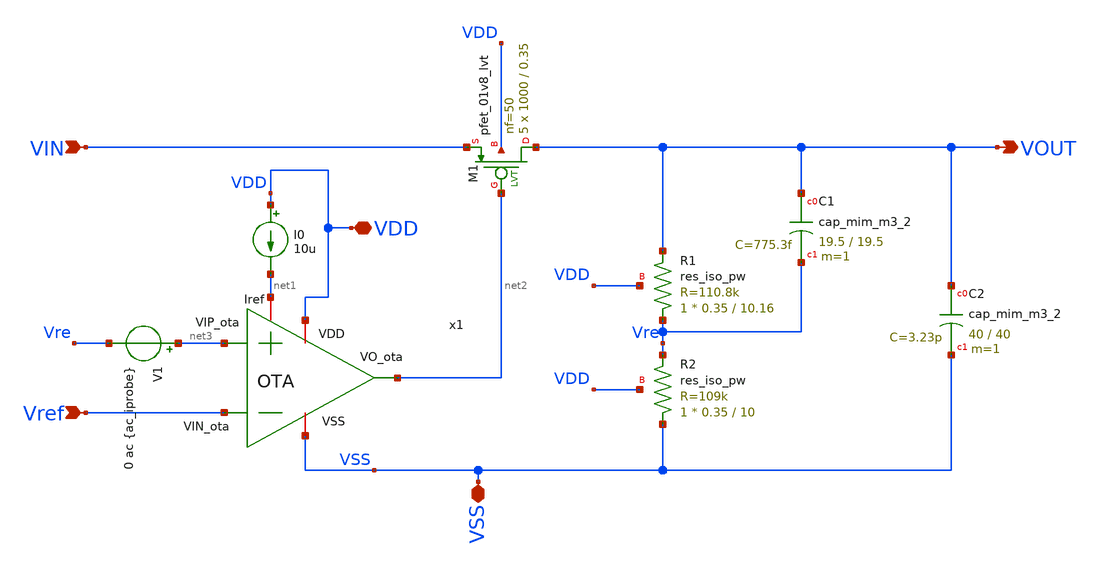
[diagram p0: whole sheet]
** sch_path: xschem/LDO.sch
**.subckt LDO VIN VDD VOUT Vref VSS
*.ipin VIN
*.iopin VDD
*.opin VOUT
*.ipin Vref
*.iopin VSS
x1 VDD net2 Vref net3 net1 VSS OTA
I0 VDD net1 10u
XM1 VOUT net2 VIN VDD sky130_fd_pr__pfet_01v8_lvt L=0.35 W=1000 nf=50 ad='int((50 + 1)/2) * 1000 / 50 * 0.29'
+ as='int((50 + 2)/2) * 1000 / 50 * 0.29' pd='2*int((50 + 1)/2) * (1000 / 50 + 0.29)' ps='2*int((50 + 2)/2) * (1000 / 50 + 0.29)'
+ nrd='0.29 / 1000 ' nrs='0.29 / 1000 ' sa=0 sb=0 sd=0 mult=5 m=5
XR1 Vre VOUT VDD sky130_fd_pr__res_iso_pw W=0.35 L=10.16 m=1
XR2 VSS Vre VDD sky130_fd_pr__res_iso_pw W=0.35 L=10 m=1
V1 net3 Vre 0 ac {ac_iprobe}
XC1 VOUT Vre sky130_fd_pr__cap_mim_m3_2 W=19.5 L=19.5 MF=1 m=1
XC2 VOUT VSS sky130_fd_pr__cap_mim_m3_2 W=40 L=40 MF=1 m=1
**.ends

* expanding   symbol:  /foss/designs/LDO-sky130/xschem/OTA.sym # of pins=6
** sym_path: xschem/OTA.sym
** sch_path: xschem/OTA.sch
.subckt OTA VDD VO_ota VIN_ota VIP_ota Iref VSS
*.ipin VIN_ota
*.opin VO_ota
*.iopin Iref
*.iopin VSS
*.iopin VDD
*.ipin VIP_ota
XR1 VO_ota1 net1 VDD sky130_fd_pr__res_high_po W=0.35 L=360 mult=1 m=1
XC1 VO_ota net1 sky130_fd_pr__cap_mim_m3_2 W=50 L=50 MF=1 m=1
XMpr VO_ota1 net2 VSS VSS sky130_fd_pr__nfet_01v8 L=0.5 W=3 nf=1 ad='int((1 + 1)/2) * 3 / 1 * 0.29' as='int((1 + 2)/2) * 3 / 1 * 0.29'
+ pd='2*int((1 + 1)/2) * (3 / 1 + 0.29)' ps='2*int((1 + 2)/2) * (3 / 1 + 0.29)' nrd='0.29 / 3 ' nrs='0.29 / 3 '
+ sa=0 sb=0 sd=0 mult=1 m=1
XMnr net2 net2 VSS VSS sky130_fd_pr__nfet_01v8 L=0.5 W=3 nf=1 ad='int((1 + 1)/2) * 3 / 1 * 0.29' as='int((1 + 2)/2) * 3 / 1 * 0.29'
+ pd='2*int((1 + 1)/2) * (3 / 1 + 0.29)' ps='2*int((1 + 2)/2) * (3 / 1 + 0.29)' nrd='0.29 / 3 ' nrs='0.29 / 3 '
+ sa=0 sb=0 sd=0 mult=1 m=1
XMn net2 VIN_ota Vtail VDD sky130_fd_pr__pfet_01v8 L=0.5 W=28 nf=1 ad='int((1 + 1)/2) * 28 / 1 * 0.29'
+ as='int((1 + 2)/2) * 28 / 1 * 0.29' pd='2*int((1 + 1)/2) * (28 / 1 + 0.29)' ps='2*int((1 + 2)/2) * (28 / 1 + 0.29)'
+ nrd='0.29 / 28 ' nrs='0.29 / 28 ' sa=0 sb=0 sd=0 mult=1 m=1
XMp VO_ota1 VIP_ota Vtail VDD sky130_fd_pr__pfet_01v8 L=0.5 W=28 nf=1 ad='int((1 + 1)/2) * 28 / 1 * 0.29'
+ as='int((1 + 2)/2) * 28 / 1 * 0.29' pd='2*int((1 + 1)/2) * (28 / 1 + 0.29)' ps='2*int((1 + 2)/2) * (28 / 1 + 0.29)'
+ nrd='0.29 / 28 ' nrs='0.29 / 28 ' sa=0 sb=0 sd=0 mult=1 m=1
XMo VO_ota VO_ota1 VSS VSS sky130_fd_pr__nfet_01v8 L=0.5 W=3 nf=1 ad='int((1 + 1)/2) * 3 / 1 * 0.29'
+ as='int((1 + 2)/2) * 3 / 1 * 0.29' pd='2*int((1 + 1)/2) * (3 / 1 + 0.29)' ps='2*int((1 + 2)/2) * (3 / 1 + 0.29)'
+ nrd='0.29 / 3 ' nrs='0.29 / 3 ' sa=0 sb=0 sd=0 mult=1 m=1
XMc3 VGP Iref VSS VSS sky130_fd_pr__nfet_01v8 L=0.5 W=1 nf=1 ad='int((1 + 1)/2) * 1 / 1 * 0.29' as='int((1 + 2)/2) * 1 / 1 * 0.29'
+ pd='2*int((1 + 1)/2) * (1 / 1 + 0.29)' ps='2*int((1 + 2)/2) * (1 / 1 + 0.29)' nrd='0.29 / 1 ' nrs='0.29 / 1 '
+ sa=0 sb=0 sd=0 mult=1 m=1
XMp2 Iref Iref VSS VSS sky130_fd_pr__nfet_01v8 L=0.5 W=1 nf=1 ad='int((1 + 1)/2) * 1 / 1 * 0.29' as='int((1 + 2)/2) * 1 / 1 * 0.29'
+ pd='2*int((1 + 1)/2) * (1 / 1 + 0.29)' ps='2*int((1 + 2)/2) * (1 / 1 + 0.29)' nrd='0.29 / 1 ' nrs='0.29 / 1 '
+ sa=0 sb=0 sd=0 mult=1 m=1
XMr VGP VGP VDD VDD sky130_fd_pr__pfet_01v8_lvt L=0.5 W=2.4 nf=1 ad='int((1 + 1)/2) * 2.4 / 1 * 0.29'
+ as='int((1 + 2)/2) * 2.4 / 1 * 0.29' pd='2*int((1 + 1)/2) * (2.4 / 1 + 0.29)' ps='2*int((1 + 2)/2) * (2.4 / 1 + 0.29)'
+ nrd='0.29 / 2.4 ' nrs='0.29 / 2.4 ' sa=0 sb=0 sd=0 mult=1 m=1
XMrc1 Vtail VGP VDD VDD sky130_fd_pr__pfet_01v8_lvt L=0.5 W=19.4 nf=1 ad='int((1 + 1)/2) * 19.4 / 1 * 0.29'
+ as='int((1 + 2)/2) * 19.4 / 1 * 0.29' pd='2*int((1 + 1)/2) * (19.4 / 1 + 0.29)' ps='2*int((1 + 2)/2) * (19.4 / 1 + 0.29)'
+ nrd='0.29 / 19.4 ' nrs='0.29 / 19.4 ' sa=0 sb=0 sd=0 mult=1 m=1
XMrc2 VO_ota VGP VDD VDD sky130_fd_pr__pfet_01v8_lvt L=0.5 W=8 nf=1 ad='int((1 + 1)/2) * 8 / 1 * 0.29'
+ as='int((1 + 2)/2) * 8 / 1 * 0.29' pd='2*int((1 + 1)/2) * (8 / 1 + 0.29)' ps='2*int((1 + 2)/2) * (8 / 1 + 0.29)'
+ nrd='0.29 / 8 ' nrs='0.29 / 8 ' sa=0 sb=0 sd=0 mult=1 m=1
.ends

.end
